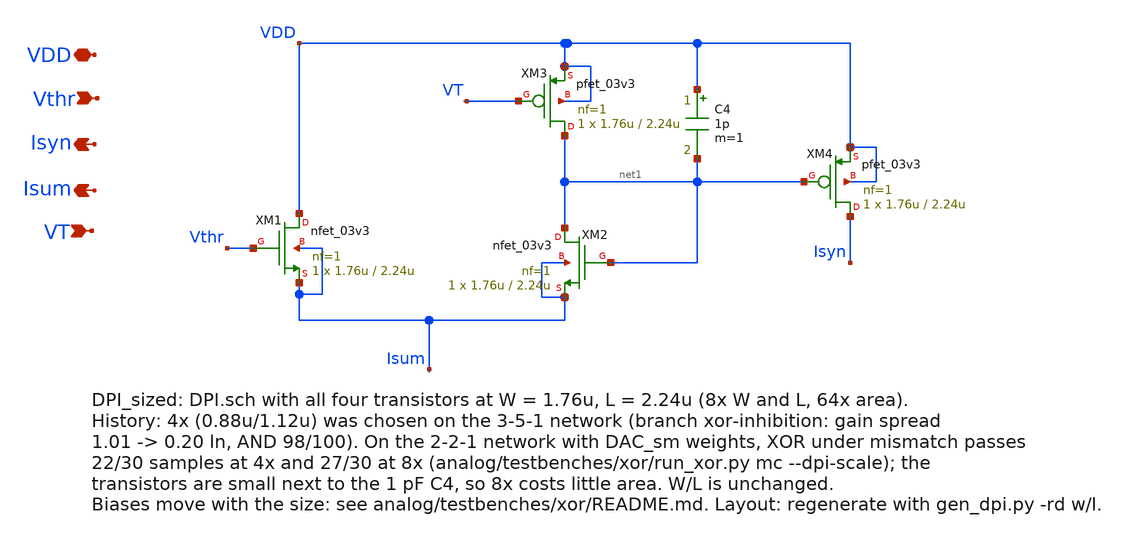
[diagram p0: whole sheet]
** sch_path: analog/neuron/DPI_sized.sch
**.subckt DPI_sized Vthr VDD Isyn Isum VT
*.ipin Vthr
*.iopin VDD
*.opin Isyn
*.opin Isum
*.ipin VT
XM1 VDD Vthr Isum Isum nfet_03v3 L=2.24u W=1.76u nf=1 ad='int((nf+1)/2) * W/nf * 0.18u' as='int((nf+2)/2) * W/nf * 0.18u'
+ pd='2*int((nf+1)/2) * (W/nf + 0.18u)' ps='2*int((nf+2)/2) * (W/nf + 0.18u)' nrd='0.18u / W' nrs='0.18u / W'
+ sa=0 sb=0 sd=0 m=1
XM2 net1 net1 Isum Isum nfet_03v3 L=2.24u W=1.76u nf=1 ad='int((nf+1)/2) * W/nf * 0.18u' as='int((nf+2)/2) * W/nf * 0.18u'
+ pd='2*int((nf+1)/2) * (W/nf + 0.18u)' ps='2*int((nf+2)/2) * (W/nf + 0.18u)' nrd='0.18u / W' nrs='0.18u / W'
+ sa=0 sb=0 sd=0 m=1
XM3 net1 VT VDD VDD pfet_03v3 L=2.24u W=1.76u nf=1 ad='int((nf+1)/2) * W/nf * 0.18u' as='int((nf+2)/2) * W/nf * 0.18u'
+ pd='2*int((nf+1)/2) * (W/nf + 0.18u)' ps='2*int((nf+2)/2) * (W/nf + 0.18u)' nrd='0.18u / W' nrs='0.18u / W'
+ sa=0 sb=0 sd=0 m=1
XM4 Isyn net1 VDD VDD pfet_03v3 L=2.24u W=1.76u nf=1 ad='int((nf+1)/2) * W/nf * 0.18u' as='int((nf+2)/2) * W/nf * 0.18u'
+ pd='2*int((nf+1)/2) * (W/nf + 0.18u)' ps='2*int((nf+2)/2) * (W/nf + 0.18u)' nrd='0.18u / W' nrs='0.18u / W'
+ sa=0 sb=0 sd=0 m=1
C4 VDD net1 1p m=1
**.ends
.end
